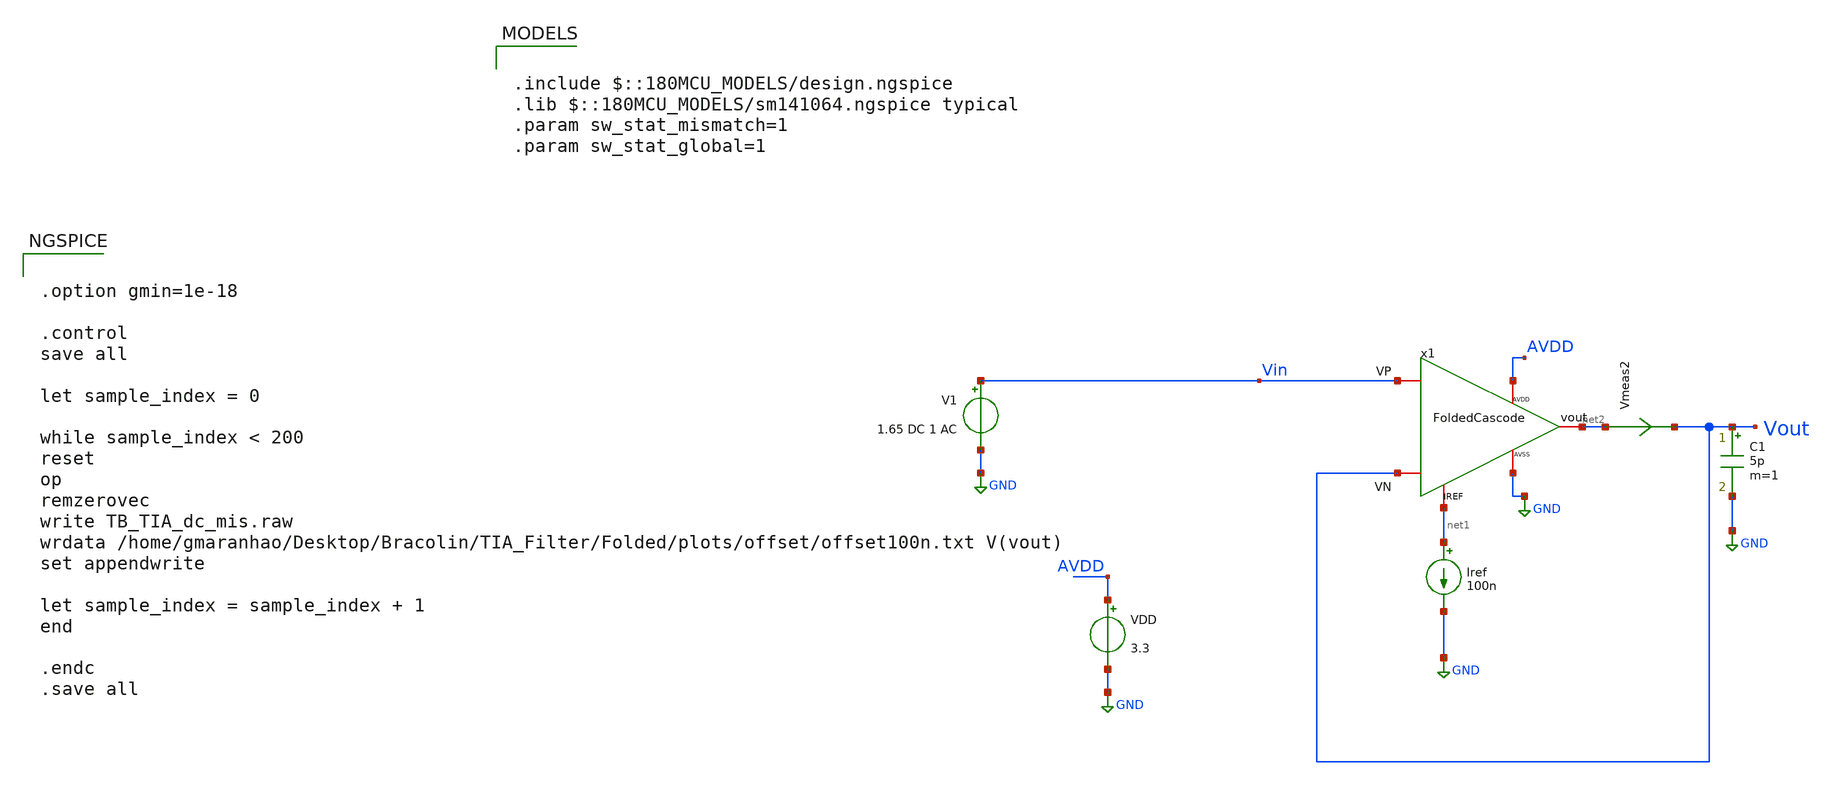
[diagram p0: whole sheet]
** sch_path: TIA_Filter/Folded/TB_Folded_dc_mis.sch
**.subckt TB_Folded_dc_mis
VDD AVDD GND 3.3
Iref net1 GND 100n
Vmeas2 net2 Vout 0
.save i(vmeas2)
C1 Vout GND 5p m=1
V1 Vin GND 1.65 DC 1 AC
x1 Vin Vout net2 net1 AVDD GND FoldedCascode
**** begin user architecture code

.include $::180MCU_MODELS/design.ngspice
.lib $::180MCU_MODELS/sm141064.ngspice typical
.param sw_stat_mismatch=1
.param sw_stat_global=1



.option gmin=1e-18

.control
save all

let sample_index = 0

while sample_index < 200
reset
op
remzerovec
write TB_TIA_dc_mis.raw
wrdata /home/gmaranhao/Desktop/Bracolin/TIA_Filter/Folded/plots/offset/offset100n.txt V(vout)
set appendwrite

let sample_index = sample_index + 1
end

.endc
.save all


**** end user architecture code
**.ends
.GLOBAL GND
.end
